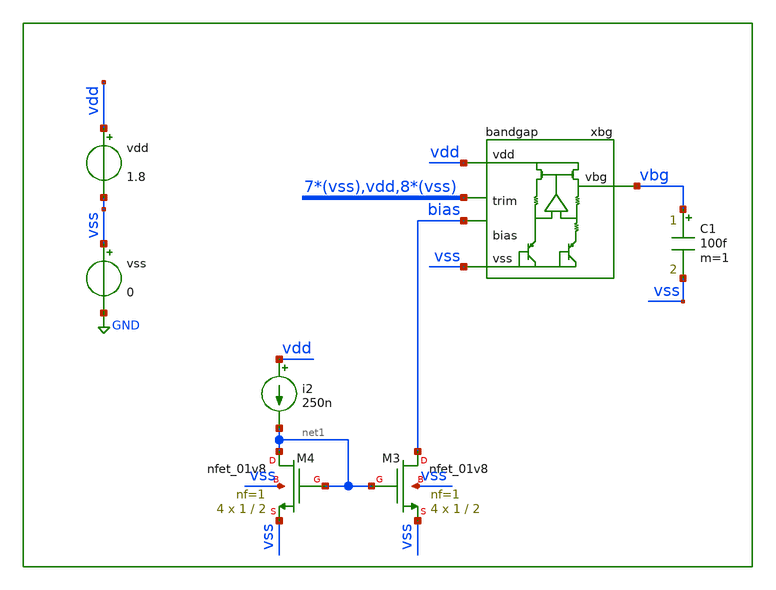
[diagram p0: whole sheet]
** sch_path: xschem/tb/bandgap/dc_bandgap_simple.sch
**.subckt dc_bandgap_simple
xbg vdd vbg vss bias vss vss vss vss vss vss vss vdd vss vss vss vss vss vss vss vss bandgap
vdd vdd vss 1.8
vss vss GND 0
C1 vbg vss 100f m=1
i2 vdd net1 250n
XM3 bias net1 vss vss sky130_fd_pr__nfet_01v8 L=2 W=1 nf=1 ad='int((nf+1)/2) * W/nf * 0.29' as='int((nf+2)/2) * W/nf * 0.29'
+ pd='2*int((nf+1)/2) * (W/nf + 0.29)' ps='2*int((nf+2)/2) * (W/nf + 0.29)' nrd='0.29 / W' nrs='0.29 / W'
+ sa=0 sb=0 sd=0 mult=4 m=4
XM4 net1 net1 vss vss sky130_fd_pr__nfet_01v8 L=2 W=1 nf=1 ad='int((nf+1)/2) * W/nf * 0.29' as='int((nf+2)/2) * W/nf * 0.29'
+ pd='2*int((nf+1)/2) * (W/nf + 0.29)' ps='2*int((nf+2)/2) * (W/nf + 0.29)' nrd='0.29 / W' nrs='0.29 / W'
+ sa=0 sb=0 sd=0 mult=4 m=4
**** begin user architecture code
*.options wnflag=1
*.options xmu=0.49
*.options method=trap
*.options reltol=0.00001
*.options vntol=1n
*.options gmin=1e-15
*.options savecurrents

.param MC_SWITCH=0

*$::DESIGN_PATH/bandgap/decoder4to16.spice
.include $::DESIGN_PATH/bandgap/bandgap.pex.spice
*.include $::DESIGN_PATH/bandgap/bandgap.ext.spice

.control
save all
dc temp -40 125 0.1
print vecmin(vbg)
print vecmax(vbg)
let delta = vecmax(vbg) - vecmin(vbg)
print delta
.endc
.end


* FET CORNERS
.include $::SKYWATER_MODELS/corners/tt.spice
*.include $::SKYWATER_MODELS/corners/ff.spice
*.include $::SKYWATER_MODELS/corners/ss.spice
*.include $::SKYWATER_MODELS/corners/sf.spice
*.include $::SKYWATER_MODELS/corners/fs.spice

* TT + R + C
*.include $::SKYWATER_MODELS/corners/tt_rmax_cmax.spice
*.include $::SKYWATER_MODELS/corners/tt_rmin_cmin.spice
*.include $::SKYWATER_MODELS/corners/tt_rmax_cmin.spice
*.include $::SKYWATER_MODELS/corners/tt_rmin_cmax.spice

* FF + R + C
*.include $::SKYWATER_MODELS/corners/ff_rmax_cmax.spice
*.include $::SKYWATER_MODELS/corners/ff_rmin_cmin.spice
*.include $::SKYWATER_MODELS/corners/ff_rmax_cmin.spice
*.include $::SKYWATER_MODELS/corners/ff_rmin_cmax.spice


* SS + R + C
*.include $::SKYWATER_MODELS/corners/ss_rmax_cmax.spice
*.include $::SKYWATER_MODELS/corners/ss_rmin_cmin.spice
*.include $::SKYWATER_MODELS/corners/ss_rmax_cmin.spice
*.include $::SKYWATER_MODELS/corners/ss_rmin_cmax.spice

* SF + R + C
*.include $::SKYWATER_MODELS/corners/sf_rmax_cmax.spice
*.include $::SKYWATER_MODELS/corners/sf_rmin_cmin.spice
*.include $::SKYWATER_MODELS/corners/sf_rmax_cmin.spice
*.include $::SKYWATER_MODELS/corners/sf_rmin_cmax.spice

* FS + R + C
*.include $::SKYWATER_MODELS/corners/fs_rmax_cmax.spice
*.include $::SKYWATER_MODELS/corners/fs_rmin_cmin.spice
*.include $::SKYWATER_MODELS/corners/fs_rmax_cmin.spice
*.include $::SKYWATER_MODELS/corners/fs_rmin_cmax.spice

**** end user architecture code
**.ends
.GLOBAL GND
.end
